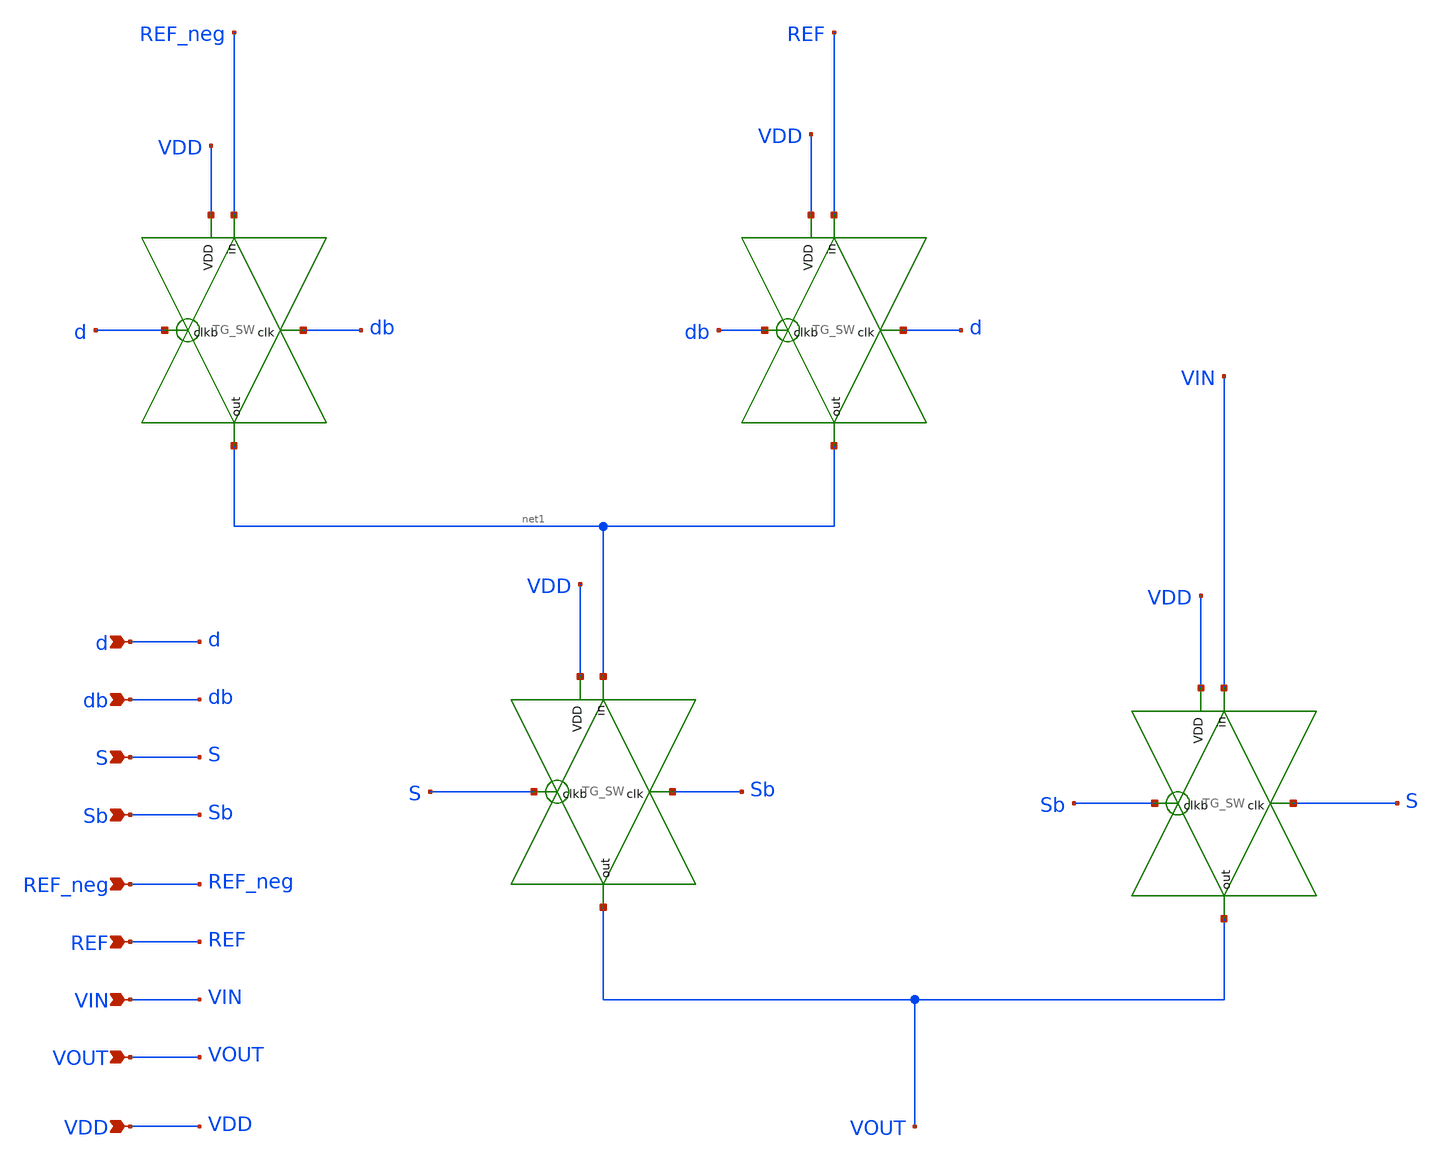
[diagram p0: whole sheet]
** sch_path: Design_Files/IC Design/Schematic/SAR_ADC_BLOCKS/SW_NW/SW_NW.sch
**.subckt SW_NW S db d Sb VIN REF REF_neg VOUT VDD
*.ipin S
*.ipin db
*.ipin d
*.ipin Sb
*.ipin VIN
*.ipin REF
*.ipin REF_neg
*.ipin VOUT
*.ipin VDD
xTGSW1 S VIN VOUT VDD Sb TG_SW
xTGSW2 Sb net1 VOUT VDD S TG_SW
xTGSW3 d REF net1 VDD db TG_SW
xTGSW4 db REF_neg net1 VDD d TG_SW
**.ends

* expanding   symbol:  ECG_Acquisition_IC/Design_Files/IC
*+ Design/Schematic/SAR_ADC_BLOCKS/TG_SW/TG_SW.sym # of pins=5
** sym_path: Design_Files/IC Design/Schematic/SAR_ADC_BLOCKS/TG_SW/TG_SW.sym
** sch_path: Design_Files/IC Design/Schematic/SAR_ADC_BLOCKS/TG_SW/TG_SW.sch
.subckt TG_SW clk in out VDD clkb
*.ipin in
*.ipin clk
*.ipin clkb
*.opin out
*.ipin VDD
XM1 out clk in 0 nfet_03v3 L=0.28u W=0.28u nf=1 ad='int((nf+1)/2) * W/nf * 0.18u' as='int((nf+2)/2) * W/nf * 0.18u'
+ pd='2*int((nf+1)/2) * (W/nf + 0.18u)' ps='2*int((nf+2)/2) * (W/nf + 0.18u)' nrd='0.18u / W' nrs='0.18u / W'
+ sa=0 sb=0 sd=0 m=1
XM2 out clkb in VDD pfet_03v3 L=0.28u W=0.28u nf=1 ad='int((nf+1)/2) * W/nf * 0.18u' as='int((nf+2)/2) * W/nf * 0.18u'
+ pd='2*int((nf+1)/2) * (W/nf + 0.18u)' ps='2*int((nf+2)/2) * (W/nf + 0.18u)' nrd='0.18u / W' nrs='0.18u / W'
+ sa=0 sb=0 sd=0 m=1
.ends

.end
